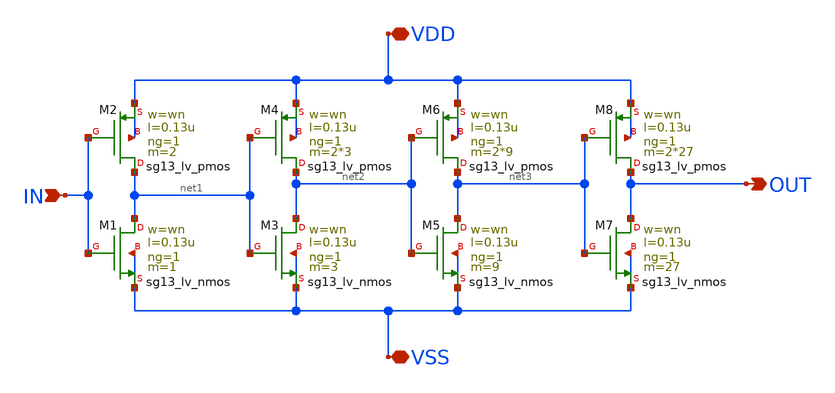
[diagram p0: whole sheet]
** sch_path: SSDOR_1.2V_v2/components/buffer4/buffer_mult.sch
**.subckt buffer_mult VDD VSS IN OUT
*.iopin VDD
*.iopin VSS
*.ipin IN
*.opin OUT
XM1 net1 IN VSS VSS sg13_lv_nmos w=wn l=0.13u ng=1 m=1 mm_ok=1
XM2 net1 IN VDD VDD sg13_lv_pmos w=wn l=0.13u ng=1 m=2 mm_ok=1
XM3 net2 net1 VSS VSS sg13_lv_nmos w=wn l=0.13u ng=1 m=3 mm_ok=1
XM4 net2 net1 VDD VDD sg13_lv_pmos w=wn l=0.13u ng=1 m=2*3 mm_ok=1
XM5 net3 net2 VSS VSS sg13_lv_nmos w=wn l=0.13u ng=1 m=9 mm_ok=1
XM6 net3 net2 VDD VDD sg13_lv_pmos w=wn l=0.13u ng=1 m=2*9 mm_ok=1
XM7 OUT net3 VSS VSS sg13_lv_nmos w=wn l=0.13u ng=1 m=27 mm_ok=1
XM8 OUT net3 VDD VDD sg13_lv_pmos w=wn l=0.13u ng=1 m=2*27 mm_ok=1
**.ends
.end
